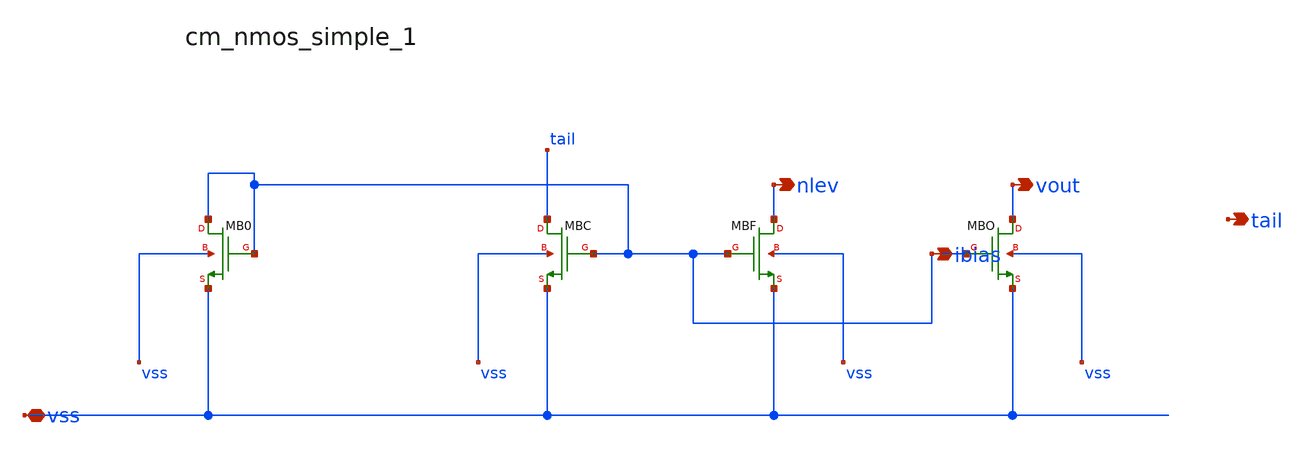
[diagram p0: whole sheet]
** sch_path: analog-db/raw/amp_032_ti_ldo_error_selfbias/hier/blocks/cm_nmos_simple_1.sch
**.subckt cm_nmos_simple_1 vss ibias nlev vout tail
*.iopin vss
*.opin ibias
*.opin nlev
*.opin vout
*.opin tail
XMB0 ibias ibias vss vss sg13_lv_nmos w=x_dut_xmb0_w l=x_dut_xmb0_l ng=1 m=1
XMBC tail ibias vss vss sg13_lv_nmos w=x_dut_xmbc_w l=x_dut_xmbc_l ng=1 m=x_dut_xmbc_m
XMBF nlev ibias vss vss sg13_lv_nmos w=x_dut_xmbf_w l=x_dut_xmbf_l ng=1 m=1
XMBO vout ibias vss vss sg13_lv_nmos w=x_dut_xmbo_w l=x_dut_xmbo_l ng=1 m=x_dut_xmbo_m
**.ends
.end
